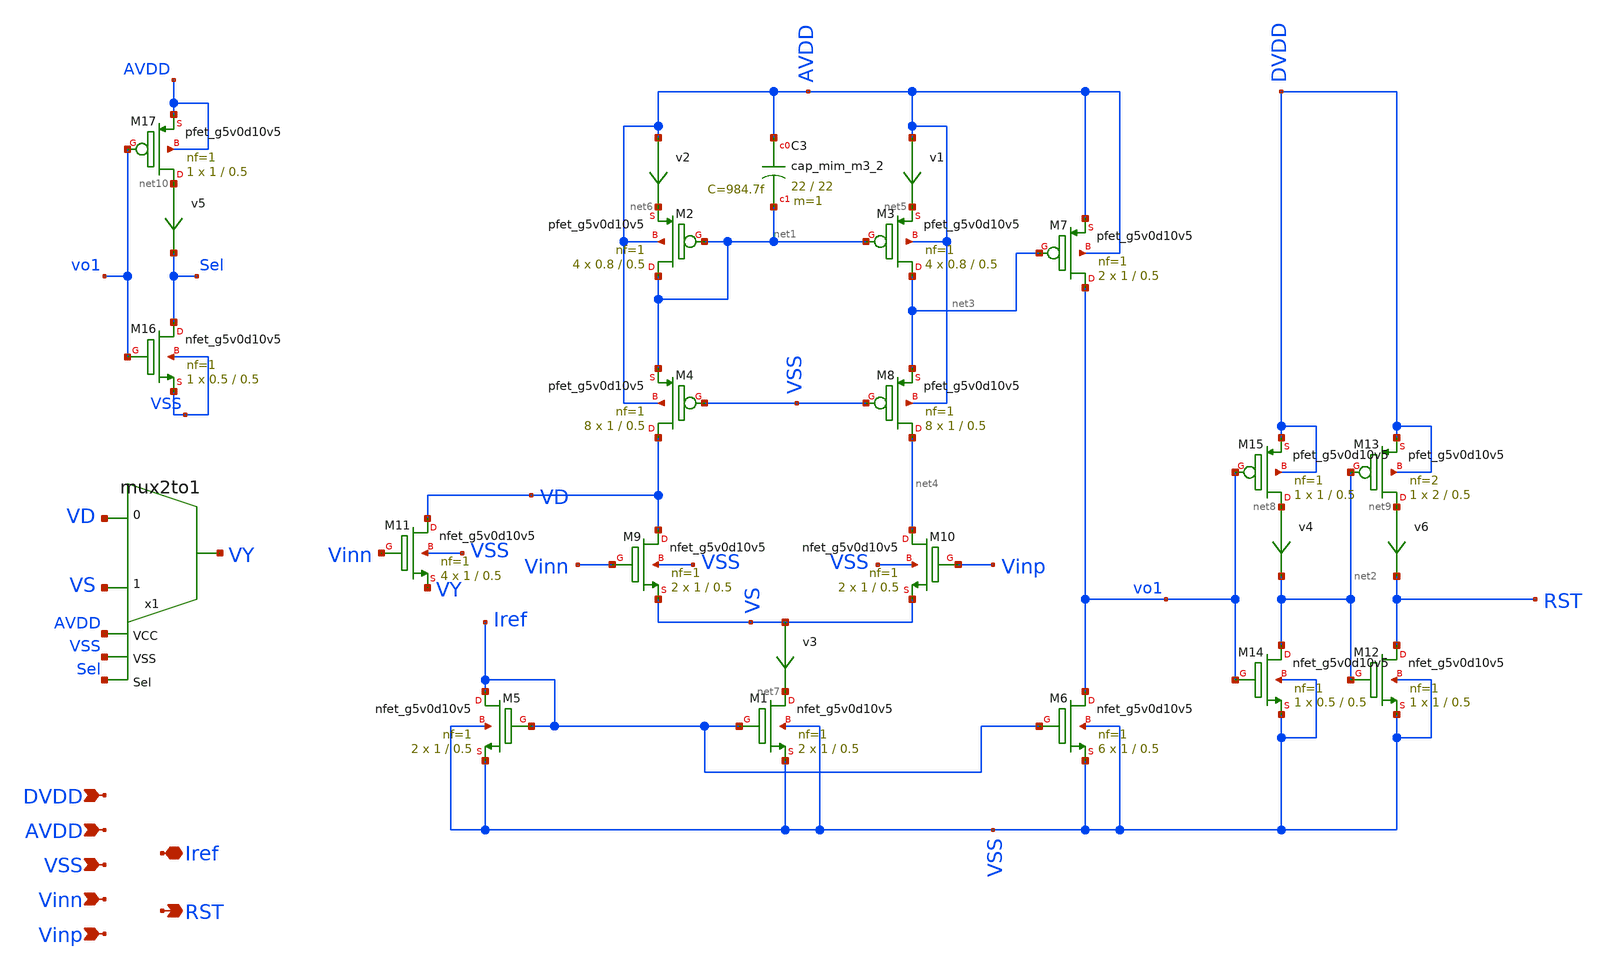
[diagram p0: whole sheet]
** sch_path: xschem/comparator.sch
**.subckt comparator AVDD RST VSS Iref Vinn Vinp DVDD
*.ipin AVDD
*.opin RST
*.ipin VSS
*.iopin Iref
*.ipin Vinn
*.ipin Vinp
*.ipin DVDD
v1 AVDD net5 0
.save i(v1)
v2 AVDD net6 0
.save i(v2)
XM1 net7 Iref VSS VSS sky130_fd_pr__nfet_g5v0d10v5 L=0.5 W=1 nf=1 ad='int((nf+1)/2) * W/nf * 0.29' as='int((nf+2)/2) * W/nf * 0.29'
+ pd='2*int((nf+1)/2) * (W/nf + 0.29)' ps='2*int((nf+2)/2) * (W/nf + 0.29)' nrd='0.29 / W' nrs='0.29 / W'
+ sa=0 sb=0 sd=0 mult=2 m=2
XM3 net3 net1 net5 AVDD sky130_fd_pr__pfet_g5v0d10v5 L=0.5 W=0.8 nf=1 ad='int((nf+1)/2) * W/nf * 0.29'
+ as='int((nf+2)/2) * W/nf * 0.29' pd='2*int((nf+1)/2) * (W/nf + 0.29)' ps='2*int((nf+2)/2) * (W/nf + 0.29)'
+ nrd='0.29 / W' nrs='0.29 / W' sa=0 sb=0 sd=0 mult=4 m=4
XM2 net1 net1 net6 AVDD sky130_fd_pr__pfet_g5v0d10v5 L=0.5 W=0.8 nf=1 ad='int((nf+1)/2) * W/nf * 0.29'
+ as='int((nf+2)/2) * W/nf * 0.29' pd='2*int((nf+1)/2) * (W/nf + 0.29)' ps='2*int((nf+2)/2) * (W/nf + 0.29)'
+ nrd='0.29 / W' nrs='0.29 / W' sa=0 sb=0 sd=0 mult=4 m=4
v4 net8 net2 0
.save i(v4)
XM9 VD Vinn VS VSS sky130_fd_pr__nfet_g5v0d10v5 L=0.5 W=1 nf=1 ad='int((nf+1)/2) * W/nf * 0.29' as='int((nf+2)/2) * W/nf * 0.29'
+ pd='2*int((nf+1)/2) * (W/nf + 0.29)' ps='2*int((nf+2)/2) * (W/nf + 0.29)' nrd='0.29 / W' nrs='0.29 / W'
+ sa=0 sb=0 sd=0 mult=2 m=2
XM10 net4 Vinp VS VSS sky130_fd_pr__nfet_g5v0d10v5 L=0.5 W=1 nf=1 ad='int((nf+1)/2) * W/nf * 0.29' as='int((nf+2)/2) * W/nf * 0.29'
+ pd='2*int((nf+1)/2) * (W/nf + 0.29)' ps='2*int((nf+2)/2) * (W/nf + 0.29)' nrd='0.29 / W' nrs='0.29 / W'
+ sa=0 sb=0 sd=0 mult=2 m=2
XM5 Iref Iref VSS VSS sky130_fd_pr__nfet_g5v0d10v5 L=0.5 W=1 nf=1 ad='int((nf+1)/2) * W/nf * 0.29' as='int((nf+2)/2) * W/nf * 0.29'
+ pd='2*int((nf+1)/2) * (W/nf + 0.29)' ps='2*int((nf+2)/2) * (W/nf + 0.29)' nrd='0.29 / W' nrs='0.29 / W'
+ sa=0 sb=0 sd=0 mult=2 m=2
XM7 vo1 net3 AVDD AVDD sky130_fd_pr__pfet_g5v0d10v5 L=0.5 W=1 nf=1 ad='int((nf+1)/2) * W/nf * 0.29' as='int((nf+2)/2) * W/nf * 0.29'
+ pd='2*int((nf+1)/2) * (W/nf + 0.29)' ps='2*int((nf+2)/2) * (W/nf + 0.29)' nrd='0.29 / W' nrs='0.29 / W'
+ sa=0 sb=0 sd=0 mult=2 m=2
v3 VS net7 0
.save i(v3)
XM11 VD Vinn VY VSS sky130_fd_pr__nfet_g5v0d10v5 L=0.5 W=1 nf=1 ad='int((nf+1)/2) * W/nf * 0.29' as='int((nf+2)/2) * W/nf * 0.29'
+ pd='2*int((nf+1)/2) * (W/nf + 0.29)' ps='2*int((nf+2)/2) * (W/nf + 0.29)' nrd='0.29 / W' nrs='0.29 / W'
+ sa=0 sb=0 sd=0 mult=4 m=4
x1 VS VD VY AVDD VSS Sel mux2to1
XM6 vo1 Iref VSS VSS sky130_fd_pr__nfet_g5v0d10v5 L=0.5 W=1 nf=1 ad='int((nf+1)/2) * W/nf * 0.29' as='int((nf+2)/2) * W/nf * 0.29'
+ pd='2*int((nf+1)/2) * (W/nf + 0.29)' ps='2*int((nf+2)/2) * (W/nf + 0.29)' nrd='0.29 / W' nrs='0.29 / W'
+ sa=0 sb=0 sd=0 mult=6 m=6
XM4 VD VSS net1 AVDD sky130_fd_pr__pfet_g5v0d10v5 L=0.5 W=1 nf=1 ad='int((nf+1)/2) * W/nf * 0.29' as='int((nf+2)/2) * W/nf * 0.29'
+ pd='2*int((nf+1)/2) * (W/nf + 0.29)' ps='2*int((nf+2)/2) * (W/nf + 0.29)' nrd='0.29 / W' nrs='0.29 / W'
+ sa=0 sb=0 sd=0 mult=8 m=8
XM8 net4 VSS net3 AVDD sky130_fd_pr__pfet_g5v0d10v5 L=0.5 W=1 nf=1 ad='int((nf+1)/2) * W/nf * 0.29' as='int((nf+2)/2) * W/nf * 0.29'
+ pd='2*int((nf+1)/2) * (W/nf + 0.29)' ps='2*int((nf+2)/2) * (W/nf + 0.29)' nrd='0.29 / W' nrs='0.29 / W'
+ sa=0 sb=0 sd=0 mult=8 m=8
v6 net9 RST 0
.save i(v6)
XM14 net2 vo1 VSS VSS sky130_fd_pr__nfet_g5v0d10v5 L=0.5 W=0.5 nf=1 ad='int((nf+1)/2) * W/nf * 0.29'
+ as='int((nf+2)/2) * W/nf * 0.29' pd='2*int((nf+1)/2) * (W/nf + 0.29)' ps='2*int((nf+2)/2) * (W/nf + 0.29)'
+ nrd='0.29 / W' nrs='0.29 / W' sa=0 sb=0 sd=0 mult=1 m=1
XM15 net8 vo1 DVDD DVDD sky130_fd_pr__pfet_g5v0d10v5 L=0.5 W=1 nf=1 ad='int((nf+1)/2) * W/nf * 0.29'
+ as='int((nf+2)/2) * W/nf * 0.29' pd='2*int((nf+1)/2) * (W/nf + 0.29)' ps='2*int((nf+2)/2) * (W/nf + 0.29)'
+ nrd='0.29 / W' nrs='0.29 / W' sa=0 sb=0 sd=0 mult=1 m=1
XM12 RST net2 VSS VSS sky130_fd_pr__nfet_g5v0d10v5 L=0.5 W=1 nf=1 ad='int((nf+1)/2) * W/nf * 0.29' as='int((nf+2)/2) * W/nf * 0.29'
+ pd='2*int((nf+1)/2) * (W/nf + 0.29)' ps='2*int((nf+2)/2) * (W/nf + 0.29)' nrd='0.29 / W' nrs='0.29 / W'
+ sa=0 sb=0 sd=0 mult=1 m=1
XM13 net9 net2 DVDD DVDD sky130_fd_pr__pfet_g5v0d10v5 L=0.5 W=2 nf=2 ad='int((nf+1)/2) * W/nf * 0.29'
+ as='int((nf+2)/2) * W/nf * 0.29' pd='2*int((nf+1)/2) * (W/nf + 0.29)' ps='2*int((nf+2)/2) * (W/nf + 0.29)'
+ nrd='0.29 / W' nrs='0.29 / W' sa=0 sb=0 sd=0 mult=1 m=1
XC3 AVDD net1 sky130_fd_pr__cap_mim_m3_2 W=22 L=22 MF=1 m=1
v5 net10 Sel 0
.save i(v5)
XM16 Sel vo1 VSS VSS sky130_fd_pr__nfet_g5v0d10v5 L=0.5 W=0.5 nf=1 ad='int((nf+1)/2) * W/nf * 0.29' as='int((nf+2)/2) * W/nf * 0.29'
+ pd='2*int((nf+1)/2) * (W/nf + 0.29)' ps='2*int((nf+2)/2) * (W/nf + 0.29)' nrd='0.29 / W' nrs='0.29 / W'
+ sa=0 sb=0 sd=0 mult=1 m=1
XM17 net10 vo1 AVDD AVDD sky130_fd_pr__pfet_g5v0d10v5 L=0.5 W=1 nf=1 ad='int((nf+1)/2) * W/nf * 0.29'
+ as='int((nf+2)/2) * W/nf * 0.29' pd='2*int((nf+1)/2) * (W/nf + 0.29)' ps='2*int((nf+2)/2) * (W/nf + 0.29)'
+ nrd='0.29 / W' nrs='0.29 / W' sa=0 sb=0 sd=0 mult=1 m=1
**.ends
.end
